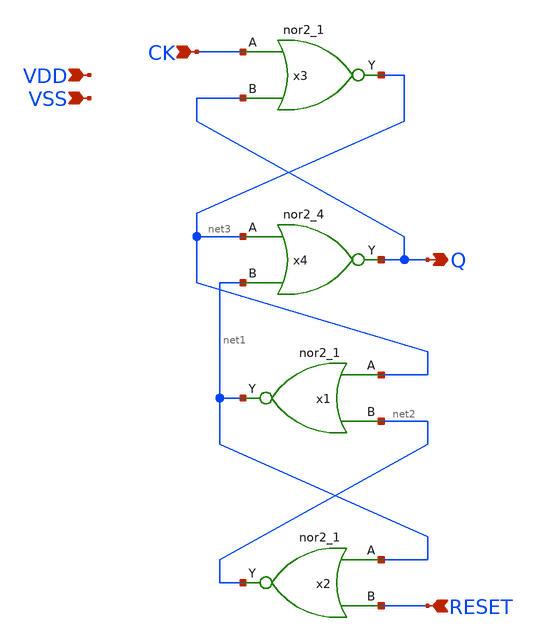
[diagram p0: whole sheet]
** sch_path: xschem/latch2.sch
**.subckt latch2 RESET CK Q VDD VSS
*.ipin RESET
*.ipin CK
*.opin Q
*.ipin VDD
*.ipin VSS
x1 net3 net2 VSS VSS VDD VDD net1 sky130_fd_sc_hd__nor2_1
x2 net1 RESET VSS VSS VDD VDD net2 sky130_fd_sc_hd__nor2_1
x3 CK Q VSS VSS VDD VDD net3 sky130_fd_sc_hd__nor2_1
x4 net3 net1 VSS VSS VDD VDD Q sky130_fd_sc_hd__nor2_4
**.ends
.end
